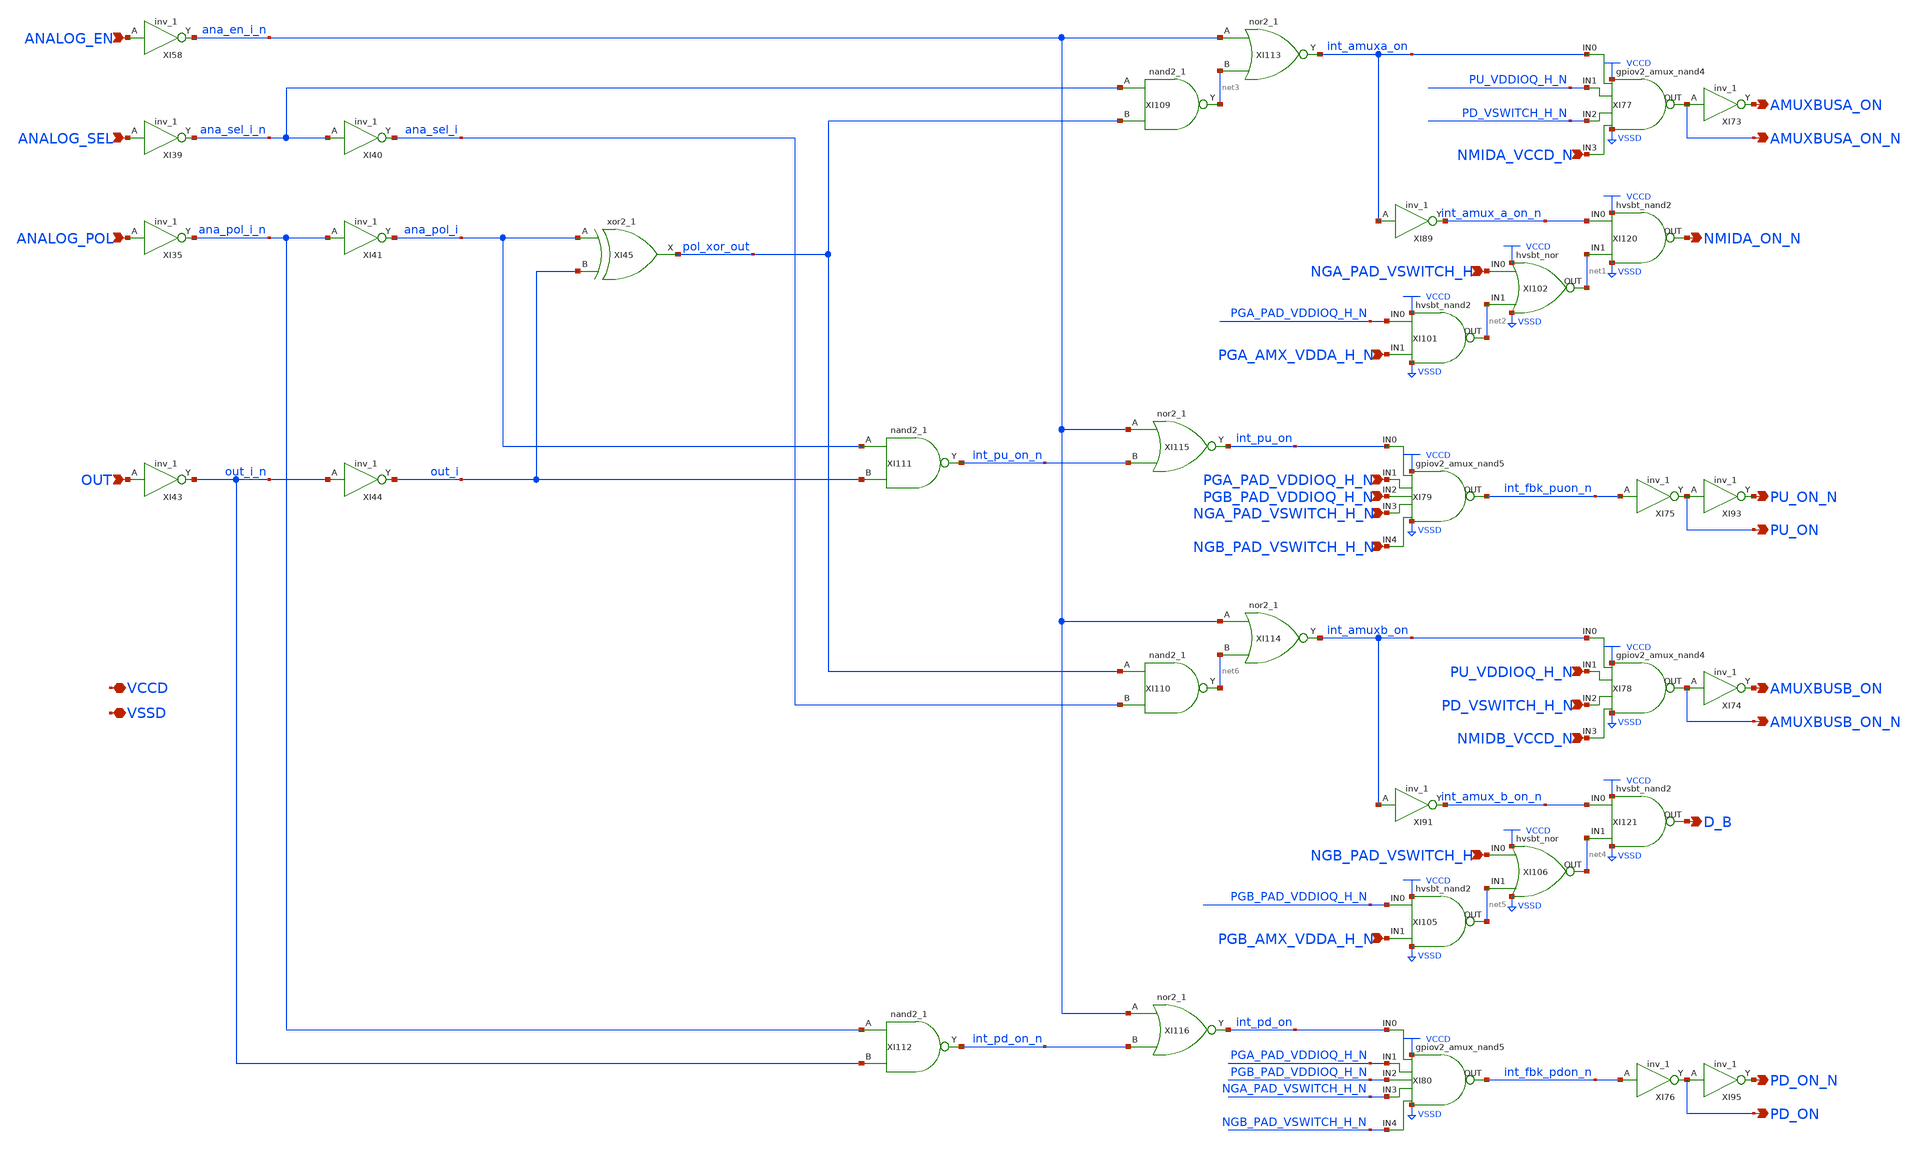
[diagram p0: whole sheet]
** sch_path: gpiov2_amux_decoder.sch
* Copyright 2023 David Mitchell Bailey
* Licensed under the Apache License, Version 2.0 (the "License");
* you may not use this file except in compliance with the License.
* You may obtain a copy of the License at
* https://www.apache.org/licenses/LICENSE-2.0
* Unless required by applicable law or agreed to in writing, software
* distributed under the License is distributed on an "AS IS" BASIS,
* WITHOUT WARRANTIES OR CONDITIONS OF ANY KIND, either express or implied.
* See the License for the specific language governing permissions and
* limitations under the License.
**.subckt gpiov2_amux_decoder ANALOG_EN VCCD PU_ON_N ANALOG_SEL ANALOG_POL OUT VSSD
*+ NGB_PAD_VSWITCH_H_N PU_ON NMIDA_VCCD_N PGA_PAD_VDDIOQ_H_N PGB_PAD_VDDIOQ_H_N NGA_PAD_VSWITCH_H_N AMUXBUSA_ON_N
*+ NGA_PAD_VSWITCH_H PGA_AMX_VDDA_H_N AMUXBUSA_ON NMIDA_ON_N PD_ON_N PD_ON PU_VDDIOQ_H_N PD_VSWITCH_H_N NMIDB_VCCD_N
*+ AMUXBUSB_ON_N NGB_PAD_VSWITCH_H PGB_AMX_VDDA_H_N AMUXBUSB_ON D_B
*.ipin ANALOG_EN
*.iopin VCCD
*.opin PU_ON_N
*.ipin ANALOG_SEL
*.ipin ANALOG_POL
*.ipin OUT
*.iopin VSSD
*.ipin NGB_PAD_VSWITCH_H_N
*.opin PU_ON
*.ipin NMIDA_VCCD_N
*.ipin PGA_PAD_VDDIOQ_H_N
*.ipin PGB_PAD_VDDIOQ_H_N
*.ipin NGA_PAD_VSWITCH_H_N
*.opin AMUXBUSA_ON_N
*.ipin NGA_PAD_VSWITCH_H
*.ipin PGA_AMX_VDDA_H_N
*.opin AMUXBUSA_ON
*.opin NMIDA_ON_N
*.opin PD_ON_N
*.opin PD_ON
*.ipin PU_VDDIOQ_H_N
*.ipin PD_VSWITCH_H_N
*.ipin NMIDB_VCCD_N
*.opin AMUXBUSB_ON_N
*.ipin NGB_PAD_VSWITCH_H
*.ipin PGB_AMX_VDDA_H_N
*.opin AMUXBUSB_ON
*.opin D_B
XI58 ANALOG_EN VSSD VSSD VCCD VCCD ana_en_i_n sky130_fd_sc_io__inv_1
XI113 ana_en_i_n net3 VSSD VSSD VCCD VCCD int_amuxa_on sky130_fd_sc_io__nor2_1
XI39 ANALOG_SEL VSSD VSSD VCCD VCCD ana_sel_i_n sky130_fd_sc_io__inv_1
XI40 ana_sel_i_n VSSD VSSD VCCD VCCD ana_sel_i sky130_fd_sc_io__inv_1
XI35 ANALOG_POL VSSD VSSD VCCD VCCD ana_pol_i_n sky130_fd_sc_io__inv_1
XI41 ana_pol_i_n VSSD VSSD VCCD VCCD ana_pol_i sky130_fd_sc_io__inv_1
XI43 OUT VSSD VSSD VCCD VCCD out_i_n sky130_fd_sc_io__inv_1
XI44 out_i_n VSSD VSSD VCCD VCCD out_i sky130_fd_sc_io__inv_1
XI45 ana_pol_i out_i VSSD VSSD VCCD VCCD pol_xor_out sky130_fd_sc_io__xor2_1
XI111 ana_pol_i out_i VSSD VSSD VCCD VCCD int_pu_on_n sky130_fd_sc_io__nand2_1
XI115 ana_en_i_n int_pu_on_n VSSD VSSD VCCD VCCD int_pu_on sky130_fd_sc_io__nor2_1
XI79 int_pu_on PGA_PAD_VDDIOQ_H_N PGB_PAD_VDDIOQ_H_N NGA_PAD_VSWITCH_H_N NGB_PAD_VSWITCH_H_N
+ int_fbk_puon_n VCCD VSSD gpiov2_amux_nand5
XI75 int_fbk_puon_n VSSD VSSD VCCD VCCD PU_ON sky130_fd_sc_io__inv_1
XI93 PU_ON VSSD VSSD VCCD VCCD PU_ON_N sky130_fd_sc_io__inv_1
XI109 ana_sel_i_n pol_xor_out VSSD VSSD VCCD VCCD net3 sky130_fd_sc_io__nand2_1
XI77 int_amuxa_on PU_VDDIOQ_H_N PD_VSWITCH_H_N NMIDA_VCCD_N AMUXBUSA_ON_N VCCD VSSD
+ gpiov2_amux_nand4
XI89 int_amuxa_on VSSD VSSD VCCD VCCD int_amux_a_on_n sky130_fd_sc_io__inv_1
XI120 int_amux_a_on_n net1 NMIDA_ON_N VCCD VSSD hvsbt_nand2
XI102 NGA_PAD_VSWITCH_H net2 net1 VCCD VSSD hvsbt_nor
XI101 PGA_PAD_VDDIOQ_H_N PGA_AMX_VDDA_H_N net2 VCCD VSSD hvsbt_nand2
XI73 AMUXBUSA_ON_N VSSD VSSD VCCD VCCD AMUXBUSA_ON sky130_fd_sc_io__inv_1
XI114 ana_en_i_n net6 VSSD VSSD VCCD VCCD int_amuxb_on sky130_fd_sc_io__nor2_1
XI112 ana_pol_i_n out_i_n VSSD VSSD VCCD VCCD int_pd_on_n sky130_fd_sc_io__nand2_1
XI116 ana_en_i_n int_pd_on_n VSSD VSSD VCCD VCCD int_pd_on sky130_fd_sc_io__nor2_1
XI80 int_pd_on PGA_PAD_VDDIOQ_H_N PGB_PAD_VDDIOQ_H_N NGA_PAD_VSWITCH_H_N NGB_PAD_VSWITCH_H_N
+ int_fbk_pdon_n VCCD VSSD gpiov2_amux_nand5
XI76 int_fbk_pdon_n VSSD VSSD VCCD VCCD PD_ON sky130_fd_sc_io__inv_1
XI95 PD_ON VSSD VSSD VCCD VCCD PD_ON_N sky130_fd_sc_io__inv_1
XI110 pol_xor_out ana_sel_i VSSD VSSD VCCD VCCD net6 sky130_fd_sc_io__nand2_1
XI78 int_amuxb_on PU_VDDIOQ_H_N PD_VSWITCH_H_N NMIDB_VCCD_N AMUXBUSB_ON_N VCCD VSSD
+ gpiov2_amux_nand4
XI91 int_amuxb_on VSSD VSSD VCCD VCCD int_amux_b_on_n sky130_fd_sc_io__inv_1
XI121 int_amux_b_on_n net4 D_B VCCD VSSD hvsbt_nand2
XI106 NGB_PAD_VSWITCH_H net5 net4 VCCD VSSD hvsbt_nor
XI105 PGB_PAD_VDDIOQ_H_N PGB_AMX_VDDA_H_N net5 VCCD VSSD hvsbt_nand2
XI74 AMUXBUSB_ON_N VSSD VSSD VCCD VCCD AMUXBUSB_ON sky130_fd_sc_io__inv_1
**.ends

* expanding   symbol:  gpiov2_amux_nand5.sym # of pins=8
** sym_path: gpiov2_amux_nand5.sym
** sch_path: gpiov2_amux_nand5.sch
.subckt gpiov2_amux_nand5 IN0 IN1 IN2 IN3 IN4 OUT VPWR VGND
*.ipin IN1
*.iopin VPWR
*.iopin VGND
*.ipin IN2
*.ipin IN0
*.ipin IN3
*.opin OUT
*.ipin IN4
XI1 OUT IN1 net2 VGND sky130_fd_pr__nfet_g5v0d10v5 L=0.5 W=5 nf=1 ad='int((nf+1)/2) * W/nf * 0.29' as='int((nf+2)/2) * W/nf * 0.29'
+ pd='2*int((nf+1)/2) * (W/nf + 0.29)' ps='2*int((nf+2)/2) * (W/nf + 0.29)' nrd='0.29 / W' nrs='0.29 / W'
+ sa=0 sb=0 sd=0 mult=1 m=1
XI3 OUT IN0 VPWR VPWR sky130_fd_pr__pfet_g5v0d10v5 L=0.6 W=2 nf=2 ad='int((nf+1)/2) * W/nf * 0.29' as='int((nf+2)/2) * W/nf * 0.29'
+ pd='2*int((nf+1)/2) * (W/nf + 0.29)' ps='2*int((nf+2)/2) * (W/nf + 0.29)' nrd='0.29 / W' nrs='0.29 / W'
+ sa=0 sb=0 sd=0 mult=1 m=1
XI2 net2 IN2 net3 VGND sky130_fd_pr__nfet_g5v0d10v5 L=0.5 W=5 nf=1 ad='int((nf+1)/2) * W/nf * 0.29' as='int((nf+2)/2) * W/nf * 0.29'
+ pd='2*int((nf+1)/2) * (W/nf + 0.29)' ps='2*int((nf+2)/2) * (W/nf + 0.29)' nrd='0.29 / W' nrs='0.29 / W'
+ sa=0 sb=0 sd=0 mult=1 m=1
XI4 net3 IN3 net4 VGND sky130_fd_pr__nfet_g5v0d10v5 L=0.5 W=5 nf=1 ad='int((nf+1)/2) * W/nf * 0.29' as='int((nf+2)/2) * W/nf * 0.29'
+ pd='2*int((nf+1)/2) * (W/nf + 0.29)' ps='2*int((nf+2)/2) * (W/nf + 0.29)' nrd='0.29 / W' nrs='0.29 / W'
+ sa=0 sb=0 sd=0 mult=1 m=1
XI5 net5 IN0 VGND VGND sky130_fd_pr__nfet_g5v0d10v5 L=0.5 W=5 nf=1 ad='int((nf+1)/2) * W/nf * 0.29' as='int((nf+2)/2) * W/nf * 0.29'
+ pd='2*int((nf+1)/2) * (W/nf + 0.29)' ps='2*int((nf+2)/2) * (W/nf + 0.29)' nrd='0.29 / W' nrs='0.29 / W'
+ sa=0 sb=0 sd=0 mult=1 m=1
XI22 net1 OUT VGND VGND sky130_fd_pr__nfet_g5v0d10v5 L=0.5 W=0.42 nf=1 ad='int((nf+1)/2) * W/nf * 0.29'
+ as='int((nf+2)/2) * W/nf * 0.29' pd='2*int((nf+1)/2) * (W/nf + 0.29)' ps='2*int((nf+2)/2) * (W/nf + 0.29)'
+ nrd='0.29 / W' nrs='0.29 / W' sa=0 sb=0 sd=0 mult=1 m=1
XI21 net1 OUT VPWR VPWR sky130_fd_pr__pfet_g5v0d10v5 L=0.6 W=2 nf=2 ad='int((nf+1)/2) * W/nf * 0.29'
+ as='int((nf+2)/2) * W/nf * 0.29' pd='2*int((nf+1)/2) * (W/nf + 0.29)' ps='2*int((nf+2)/2) * (W/nf + 0.29)'
+ nrd='0.29 / W' nrs='0.29 / W' sa=0 sb=0 sd=0 mult=1 m=1
XI23 VGND net1 VGND VGND sky130_fd_pr__nfet_g5v0d10v5 L=0.5 W=0.42 nf=1 ad='int((nf+1)/2) * W/nf * 0.29'
+ as='int((nf+2)/2) * W/nf * 0.29' pd='2*int((nf+1)/2) * (W/nf + 0.29)' ps='2*int((nf+2)/2) * (W/nf + 0.29)'
+ nrd='0.29 / W' nrs='0.29 / W' sa=0 sb=0 sd=0 mult=1 m=1
XI20 OUT net1 VPWR VPWR sky130_fd_pr__pfet_g5v0d10v5 L=0.5 W=0.42 nf=1 ad='int((nf+1)/2) * W/nf * 0.29'
+ as='int((nf+2)/2) * W/nf * 0.29' pd='2*int((nf+1)/2) * (W/nf + 0.29)' ps='2*int((nf+2)/2) * (W/nf + 0.29)'
+ nrd='0.29 / W' nrs='0.29 / W' sa=0 sb=0 sd=0 mult=1 m=1
XI18 net4 IN4 net5 VGND sky130_fd_pr__nfet_g5v0d10v5 L=0.5 W=5 nf=1 ad='int((nf+1)/2) * W/nf * 0.29'
+ as='int((nf+2)/2) * W/nf * 0.29' pd='2*int((nf+1)/2) * (W/nf + 0.29)' ps='2*int((nf+2)/2) * (W/nf + 0.29)'
+ nrd='0.29 / W' nrs='0.29 / W' sa=0 sb=0 sd=0 mult=1 m=1
.ends


* expanding   symbol:  gpiov2_amux_nand4.sym # of pins=7
** sym_path: gpiov2_amux_nand4.sym
** sch_path: gpiov2_amux_nand4.sch
.subckt gpiov2_amux_nand4 IN0 IN1 IN2 IN3 OUT VPWR VGND
*.ipin IN1
*.iopin VPWR
*.iopin VGND
*.ipin IN2
*.ipin IN0
*.ipin IN3
*.opin OUT
XI1 OUT IN1 net2 VGND sky130_fd_pr__nfet_g5v0d10v5 L=0.5 W=5 nf=1 ad='int((nf+1)/2) * W/nf * 0.29' as='int((nf+2)/2) * W/nf * 0.29'
+ pd='2*int((nf+1)/2) * (W/nf + 0.29)' ps='2*int((nf+2)/2) * (W/nf + 0.29)' nrd='0.29 / W' nrs='0.29 / W'
+ sa=0 sb=0 sd=0 mult=1 m=1
XI3 OUT IN0 VPWR VPWR sky130_fd_pr__pfet_g5v0d10v5 L=0.6 W=2 nf=2 ad='int((nf+1)/2) * W/nf * 0.29' as='int((nf+2)/2) * W/nf * 0.29'
+ pd='2*int((nf+1)/2) * (W/nf + 0.29)' ps='2*int((nf+2)/2) * (W/nf + 0.29)' nrd='0.29 / W' nrs='0.29 / W'
+ sa=0 sb=0 sd=0 mult=1 m=1
XI2 net2 IN2 net3 VGND sky130_fd_pr__nfet_g5v0d10v5 L=0.5 W=5 nf=1 ad='int((nf+1)/2) * W/nf * 0.29' as='int((nf+2)/2) * W/nf * 0.29'
+ pd='2*int((nf+1)/2) * (W/nf + 0.29)' ps='2*int((nf+2)/2) * (W/nf + 0.29)' nrd='0.29 / W' nrs='0.29 / W'
+ sa=0 sb=0 sd=0 mult=1 m=1
XI4 net3 IN3 net4 VGND sky130_fd_pr__nfet_g5v0d10v5 L=0.5 W=5 nf=1 ad='int((nf+1)/2) * W/nf * 0.29' as='int((nf+2)/2) * W/nf * 0.29'
+ pd='2*int((nf+1)/2) * (W/nf + 0.29)' ps='2*int((nf+2)/2) * (W/nf + 0.29)' nrd='0.29 / W' nrs='0.29 / W'
+ sa=0 sb=0 sd=0 mult=1 m=1
XI5 net4 IN0 VGND VGND sky130_fd_pr__nfet_g5v0d10v5 L=0.5 W=5 nf=1 ad='int((nf+1)/2) * W/nf * 0.29' as='int((nf+2)/2) * W/nf * 0.29'
+ pd='2*int((nf+1)/2) * (W/nf + 0.29)' ps='2*int((nf+2)/2) * (W/nf + 0.29)' nrd='0.29 / W' nrs='0.29 / W'
+ sa=0 sb=0 sd=0 mult=1 m=1
XI18 net1 OUT VGND VGND sky130_fd_pr__nfet_g5v0d10v5 L=0.5 W=0.42 nf=1 ad='int((nf+1)/2) * W/nf * 0.29'
+ as='int((nf+2)/2) * W/nf * 0.29' pd='2*int((nf+1)/2) * (W/nf + 0.29)' ps='2*int((nf+2)/2) * (W/nf + 0.29)'
+ nrd='0.29 / W' nrs='0.29 / W' sa=0 sb=0 sd=0 mult=1 m=1
XI6 net1 OUT VPWR VPWR sky130_fd_pr__pfet_g5v0d10v5 L=0.6 W=2 nf=2 ad='int((nf+1)/2) * W/nf * 0.29' as='int((nf+2)/2) * W/nf * 0.29'
+ pd='2*int((nf+1)/2) * (W/nf + 0.29)' ps='2*int((nf+2)/2) * (W/nf + 0.29)' nrd='0.29 / W' nrs='0.29 / W'
+ sa=0 sb=0 sd=0 mult=1 m=1
XI7 VGND net1 VGND VGND sky130_fd_pr__nfet_g5v0d10v5 L=0.5 W=0.42 nf=1 ad='int((nf+1)/2) * W/nf * 0.29'
+ as='int((nf+2)/2) * W/nf * 0.29' pd='2*int((nf+1)/2) * (W/nf + 0.29)' ps='2*int((nf+2)/2) * (W/nf + 0.29)'
+ nrd='0.29 / W' nrs='0.29 / W' sa=0 sb=0 sd=0 mult=1 m=1
XI20 OUT net1 VPWR VPWR sky130_fd_pr__pfet_g5v0d10v5 L=0.5 W=0.42 nf=1 ad='int((nf+1)/2) * W/nf * 0.29'
+ as='int((nf+2)/2) * W/nf * 0.29' pd='2*int((nf+1)/2) * (W/nf + 0.29)' ps='2*int((nf+2)/2) * (W/nf + 0.29)'
+ nrd='0.29 / W' nrs='0.29 / W' sa=0 sb=0 sd=0 mult=1 m=1
.ends


* expanding   symbol:  common/hvsbt_nand2.sym # of pins=5
** sym_path: common/hvsbt_nand2.sym
** sch_path: common/hvsbt_nand2.sch
.subckt hvsbt_nand2 IN0 IN1 OUT VPWR VGND
*.ipin IN1
*.opin OUT
*.iopin VPWR
*.iopin VGND
*.ipin IN0
XI1 OUT IN1 net1 VGND sky130_fd_pr__nfet_g5v0d10v5 L=0.6 W=0.7 nf=1 ad='int((nf+1)/2) * W/nf * 0.29'
+ as='int((nf+2)/2) * W/nf * 0.29' pd='2*int((nf+1)/2) * (W/nf + 0.29)' ps='2*int((nf+2)/2) * (W/nf + 0.29)'
+ nrd='0.29 / W' nrs='0.29 / W' sa=0 sb=0 sd=0 mult=1 m=1
XI5 OUT IN1 VPWR VPWR sky130_fd_pr__pfet_g5v0d10v5 L=0.6 W=1 nf=1 ad='int((nf+1)/2) * W/nf * 0.29' as='int((nf+2)/2) * W/nf * 0.29'
+ pd='2*int((nf+1)/2) * (W/nf + 0.29)' ps='2*int((nf+2)/2) * (W/nf + 0.29)' nrd='0.29 / W' nrs='0.29 / W'
+ sa=0 sb=0 sd=0 mult=2 m=2
XI3 OUT IN0 VPWR VPWR sky130_fd_pr__pfet_g5v0d10v5 L=0.6 W=1 nf=1 ad='int((nf+1)/2) * W/nf * 0.29' as='int((nf+2)/2) * W/nf * 0.29'
+ pd='2*int((nf+1)/2) * (W/nf + 0.29)' ps='2*int((nf+2)/2) * (W/nf + 0.29)' nrd='0.29 / W' nrs='0.29 / W'
+ sa=0 sb=0 sd=0 mult=2 m=2
XI6 net1 IN0 VGND VGND sky130_fd_pr__nfet_g5v0d10v5 L=0.6 W=0.7 nf=1 ad='int((nf+1)/2) * W/nf * 0.29'
+ as='int((nf+2)/2) * W/nf * 0.29' pd='2*int((nf+1)/2) * (W/nf + 0.29)' ps='2*int((nf+2)/2) * (W/nf + 0.29)'
+ nrd='0.29 / W' nrs='0.29 / W' sa=0 sb=0 sd=0 mult=1 m=1
.ends


* expanding   symbol:  common/hvsbt_nor.sym # of pins=5
** sym_path: common/hvsbt_nor.sym
** sch_path: common/hvsbt_nor.sch
.subckt hvsbt_nor IN0 IN1 OUT VPWR VGND
*.ipin IN1
*.opin OUT
*.iopin VPWR
*.iopin VGND
*.ipin IN0
XI2 OUT IN1 VGND VGND sky130_fd_pr__nfet_g5v0d10v5 L=0.6 W=0.7 nf=1 ad='int((nf+1)/2) * W/nf * 0.29'
+ as='int((nf+2)/2) * W/nf * 0.29' pd='2*int((nf+1)/2) * (W/nf + 0.29)' ps='2*int((nf+2)/2) * (W/nf + 0.29)'
+ nrd='0.29 / W' nrs='0.29 / W' sa=0 sb=0 sd=0 mult=1 m=1
XI1 OUT IN1 net1 VPWR sky130_fd_pr__pfet_g5v0d10v5 L=0.6 W=1 nf=1 ad='int((nf+1)/2) * W/nf * 0.29' as='int((nf+2)/2) * W/nf * 0.29'
+ pd='2*int((nf+1)/2) * (W/nf + 0.29)' ps='2*int((nf+2)/2) * (W/nf + 0.29)' nrd='0.29 / W' nrs='0.29 / W'
+ sa=0 sb=0 sd=0 mult=2 m=2
XI3 net1 IN0 VPWR VPWR sky130_fd_pr__pfet_g5v0d10v5 L=0.6 W=1 nf=1 ad='int((nf+1)/2) * W/nf * 0.29' as='int((nf+2)/2) * W/nf * 0.29'
+ pd='2*int((nf+1)/2) * (W/nf + 0.29)' ps='2*int((nf+2)/2) * (W/nf + 0.29)' nrd='0.29 / W' nrs='0.29 / W'
+ sa=0 sb=0 sd=0 mult=2 m=2
XI4 OUT IN0 VGND VGND sky130_fd_pr__nfet_g5v0d10v5 L=0.6 W=0.7 nf=1 ad='int((nf+1)/2) * W/nf * 0.29'
+ as='int((nf+2)/2) * W/nf * 0.29' pd='2*int((nf+1)/2) * (W/nf + 0.29)' ps='2*int((nf+2)/2) * (W/nf + 0.29)'
+ nrd='0.29 / W' nrs='0.29 / W' sa=0 sb=0 sd=0 mult=1 m=1
.ends

.end
